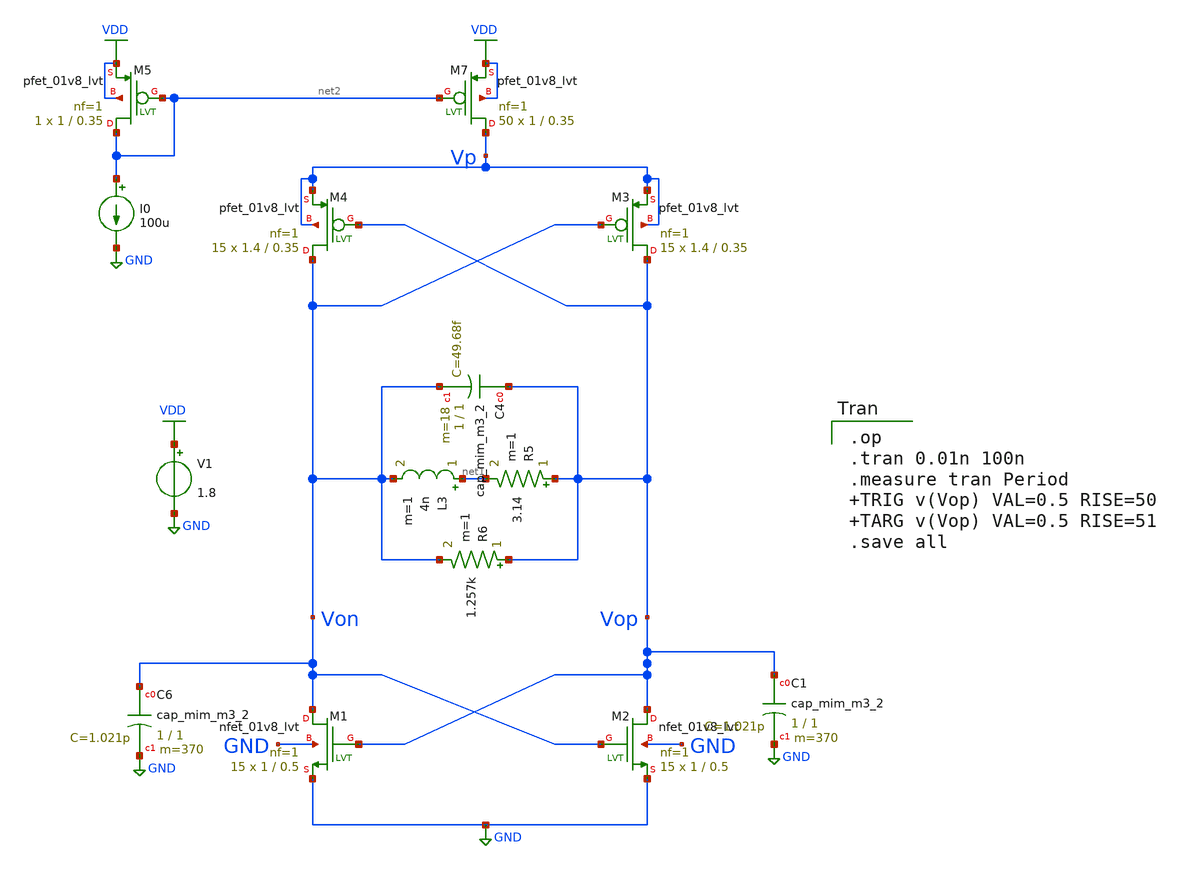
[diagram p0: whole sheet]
** sch_path: pll/lc_vco_lib_Hossam_Tarek/lc_osc_complementary_pmos_tb/xschem/lc_osc_complementary_pmos_tb.sch
**.subckt lc_osc_complementary_pmos_tb
XM1 Von Vop GND GND sky130_fd_pr__nfet_01v8_lvt L=0.5 W=1 nf=1 ad='int((nf+1)/2) * W/nf * 0.29' as='int((nf+2)/2) * W/nf * 0.29'
+ pd='2*int((nf+1)/2) * (W/nf + 0.29)' ps='2*int((nf+2)/2) * (W/nf + 0.29)' nrd='0.29 / W' nrs='0.29 / W'
+ sa=0 sb=0 sd=0 mult=15 m=15
XM2 Vop Von GND GND sky130_fd_pr__nfet_01v8_lvt L=0.5 W=1 nf=1 ad='int((nf+1)/2) * W/nf * 0.29' as='int((nf+2)/2) * W/nf * 0.29'
+ pd='2*int((nf+1)/2) * (W/nf + 0.29)' ps='2*int((nf+2)/2) * (W/nf + 0.29)' nrd='0.29 / W' nrs='0.29 / W'
+ sa=0 sb=0 sd=0 mult=15 m=15
V1 VDD GND 1.8
XC6 Von GND sky130_fd_pr__cap_mim_m3_2 W=1 L=1 MF=370 m=370
XC1 Vop GND sky130_fd_pr__cap_mim_m3_2 W=1 L=1 MF=370 m=370
L3 net1 Von 4n m=1
R5 Vop net1 3.14 m=1
R6 Vop Von 1.257k m=1
XC4 Vop Von sky130_fd_pr__cap_mim_m3_2 W=1 L=1 MF=18 m=18
XM3 Vop Von Vp Vp sky130_fd_pr__pfet_01v8_lvt L=0.35 W=1.4 nf=1 ad='int((nf+1)/2) * W/nf * 0.29' as='int((nf+2)/2) * W/nf * 0.29'
+ pd='2*int((nf+1)/2) * (W/nf + 0.29)' ps='2*int((nf+2)/2) * (W/nf + 0.29)' nrd='0.29 / W' nrs='0.29 / W'
+ sa=0 sb=0 sd=0 mult=15 m=15
XM4 Von Vop Vp Vp sky130_fd_pr__pfet_01v8_lvt L=0.35 W=1.4 nf=1 ad='int((nf+1)/2) * W/nf * 0.29' as='int((nf+2)/2) * W/nf * 0.29'
+ pd='2*int((nf+1)/2) * (W/nf + 0.29)' ps='2*int((nf+2)/2) * (W/nf + 0.29)' nrd='0.29 / W' nrs='0.29 / W'
+ sa=0 sb=0 sd=0 mult=15 m=15
I0 net2 GND 100u
XM7 Vp net2 VDD VDD sky130_fd_pr__pfet_01v8_lvt L=0.35 W=1 nf=1 ad='int((nf+1)/2) * W/nf * 0.29' as='int((nf+2)/2) * W/nf * 0.29'
+ pd='2*int((nf+1)/2) * (W/nf + 0.29)' ps='2*int((nf+2)/2) * (W/nf + 0.29)' nrd='0.29 / W' nrs='0.29 / W'
+ sa=0 sb=0 sd=0 mult=50 m=50
XM5 net2 net2 VDD VDD sky130_fd_pr__pfet_01v8_lvt L=0.35 W=1 nf=1 ad='int((nf+1)/2) * W/nf * 0.29' as='int((nf+2)/2) * W/nf * 0.29'
+ pd='2*int((nf+1)/2) * (W/nf + 0.29)' ps='2*int((nf+2)/2) * (W/nf + 0.29)' nrd='0.29 / W' nrs='0.29 / W'
+ sa=0 sb=0 sd=0 mult=1 m=1
**** begin user architecture code

.op
.tran 0.01n 100n
.measure tran Period  TRIG v(Vop) VAL=0.5 RISE=50  TARG v(Vop) VAL=0.5 RISE=51
.save all


** opencircuitdesign pdks install
.lib $::SKYWATER_MODELS/sky130.lib.spice tt


**** end user architecture code
**.ends
.GLOBAL GND
.GLOBAL VDD
.end
